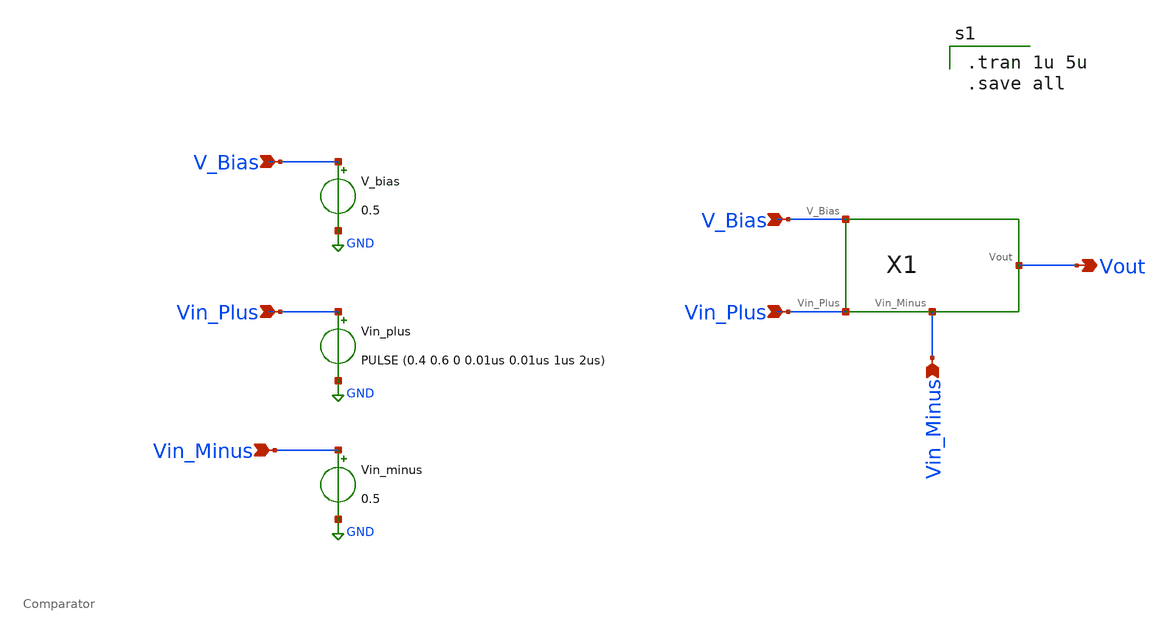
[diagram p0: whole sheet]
** sch_path: Current Sensor/Comparator_test_bed.sch
**.subckt Comparator_test_bed V_Bias Vin_Plus Vin_Minus Vout V_Bias Vin_Plus Vin_Minus
*.ipin V_Bias
*.ipin Vin_Plus
*.ipin Vin_Minus
*.opin Vout
*.ipin V_Bias
*.ipin Vin_Plus
*.ipin Vin_Minus
X1 V_Bias Vin_Plus Vin_Minus Vout Comparator
V_bias V_Bias GND 0.5
Vin_plus Vin_Plus GND PULSE (0.4 0.6 0 0.01us 0.01us 1us 2us)
Vin_minus Vin_Minus GND 0.5
**** begin user architecture code
** manual skywater pdks install (with patches applied)
* .lib $::SKYWATER_MODELS/models/sky130.lib.spice tt_mm

** opencircuitdesign pdks install
.lib $::SKYWATER_MODELS/sky130.lib.spice tt_mm



.tran 1u 5u
.save all

**** end user architecture code
**.ends

* expanding   symbol:  Comparator.sym # of pins=4
** sym_path: Current Sensor/Comparator.sym
** sch_path: Current Sensor/Comparator.sch
.subckt Comparator V_Bias Vin_Plus Vin_Minus Vout
*.ipin V_Bias
*.ipin Vin_Plus
*.ipin Vin_Minus
*.opin Vout
XM1 net1 net1 VDD VDD sky130_fd_pr__pfet_01v8_lvt L=0.35 W=1 nf=1 ad='int((nf+1)/2) * W/nf * 0.29' as='int((nf+2)/2) * W/nf * 0.29'
+ pd='2*int((nf+1)/2) * (W/nf + 0.29)' ps='2*int((nf+2)/2) * (W/nf + 0.29)' nrd='0.29 / W' nrs='0.29 / W'
+ sa=0 sb=0 sd=0 mult=1 m=1
XM2 net2 net1 VDD VDD sky130_fd_pr__pfet_01v8_lvt L=0.35 W=1 nf=1 ad='int((nf+1)/2) * W/nf * 0.29' as='int((nf+2)/2) * W/nf * 0.29'
+ pd='2*int((nf+1)/2) * (W/nf + 0.29)' ps='2*int((nf+2)/2) * (W/nf + 0.29)' nrd='0.29 / W' nrs='0.29 / W'
+ sa=0 sb=0 sd=0 mult=1 m=1
XM3 Vout net2 VDD VDD sky130_fd_pr__pfet_01v8_lvt L=0.35 W=1 nf=1 ad='int((nf+1)/2) * W/nf * 0.29' as='int((nf+2)/2) * W/nf * 0.29'
+ pd='2*int((nf+1)/2) * (W/nf + 0.29)' ps='2*int((nf+2)/2) * (W/nf + 0.29)' nrd='0.29 / W' nrs='0.29 / W'
+ sa=0 sb=0 sd=0 mult=1 m=1
XM4 net3 V_Bias GND GND sky130_fd_pr__nfet_01v8_lvt L=0.15 W=1 nf=1 ad='int((nf+1)/2) * W/nf * 0.29'
+ as='int((nf+2)/2) * W/nf * 0.29' pd='2*int((nf+1)/2) * (W/nf + 0.29)' ps='2*int((nf+2)/2) * (W/nf + 0.29)'
+ nrd='0.29 / W' nrs='0.29 / W' sa=0 sb=0 sd=0 mult=1 m=1
XM5 Vout V_Bias GND GND sky130_fd_pr__nfet_01v8_lvt L=0.15 W=1 nf=1 ad='int((nf+1)/2) * W/nf * 0.29'
+ as='int((nf+2)/2) * W/nf * 0.29' pd='2*int((nf+1)/2) * (W/nf + 0.29)' ps='2*int((nf+2)/2) * (W/nf + 0.29)'
+ nrd='0.29 / W' nrs='0.29 / W' sa=0 sb=0 sd=0 mult=1 m=1
XM6 net1 Vin_Minus net3 net3 sky130_fd_pr__nfet_01v8_lvt L=0.15 W=1 nf=1 ad='int((nf+1)/2) * W/nf * 0.29'
+ as='int((nf+2)/2) * W/nf * 0.29' pd='2*int((nf+1)/2) * (W/nf + 0.29)' ps='2*int((nf+2)/2) * (W/nf + 0.29)'
+ nrd='0.29 / W' nrs='0.29 / W' sa=0 sb=0 sd=0 mult=1 m=1
XM7 net2 Vin_Plus net3 net3 sky130_fd_pr__nfet_01v8_lvt L=0.15 W=1 nf=1 ad='int((nf+1)/2) * W/nf * 0.29'
+ as='int((nf+2)/2) * W/nf * 0.29' pd='2*int((nf+1)/2) * (W/nf + 0.29)' ps='2*int((nf+2)/2) * (W/nf + 0.29)'
+ nrd='0.29 / W' nrs='0.29 / W' sa=0 sb=0 sd=0 mult=1 m=1
V1 VDD GND 1.8
.ends

.GLOBAL GND
.GLOBAL VDD
.end
